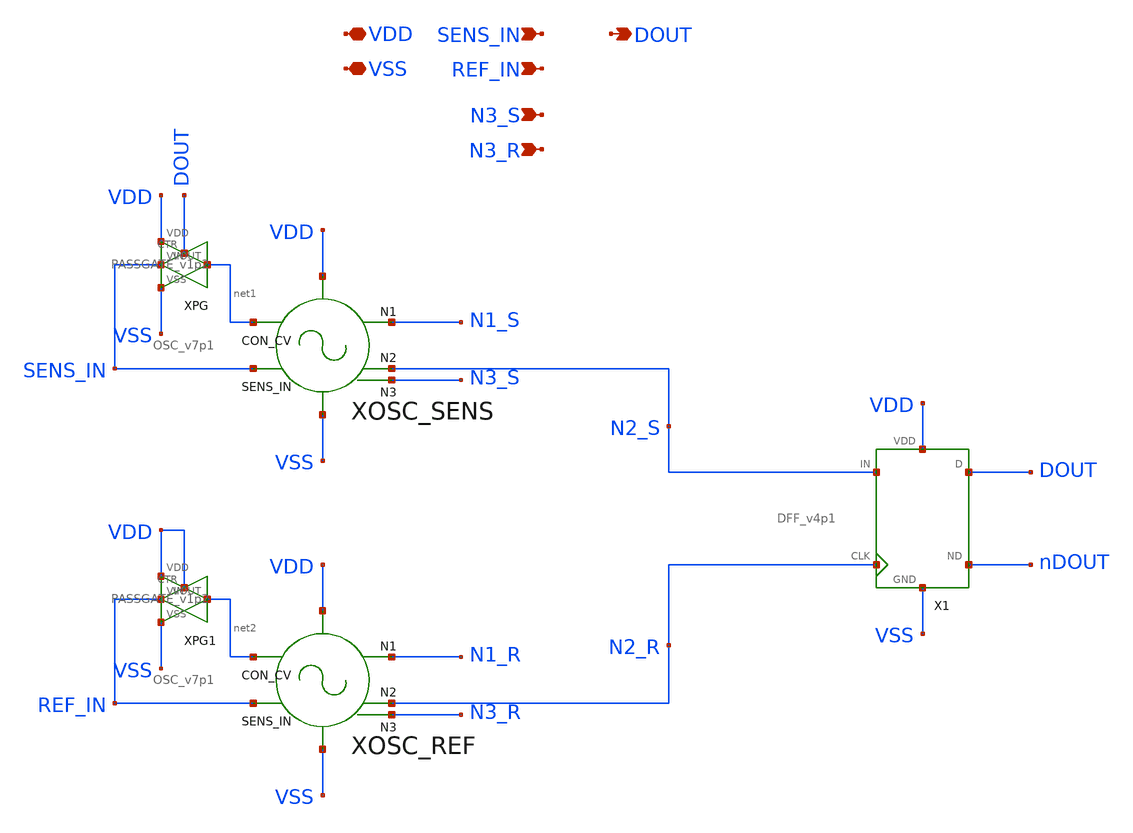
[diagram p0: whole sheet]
** sch_path: modules/SDC_v7p1_ROrangeext/symbol/SDC_v7p1_ROrangeext.sch
**.subckt SDC_v7p1_ROrangeext VDD VSS SENS_IN REF_IN DOUT N3_S N3_R
*.iopin VDD
*.iopin VSS
*.ipin SENS_IN
*.ipin REF_IN
*.opin DOUT
*.ipin N3_S
*.ipin N3_R
XOSC_SENS SENS_IN N1_S N2_S VDD VSS net1 N3_S OSC_v7p1
XOSC_REF REF_IN N1_R N2_R VDD VSS net2 N3_R OSC_v7p1
XPG SENS_IN DOUT net1 VDD VSS PASSGATE_v1p2
XPG1 REF_IN VDD net2 VDD VSS PASSGATE_v1p2
X1 N2_S N2_R DOUT nDOUT VDD VSS DFF_v4p1
**.ends
.end
